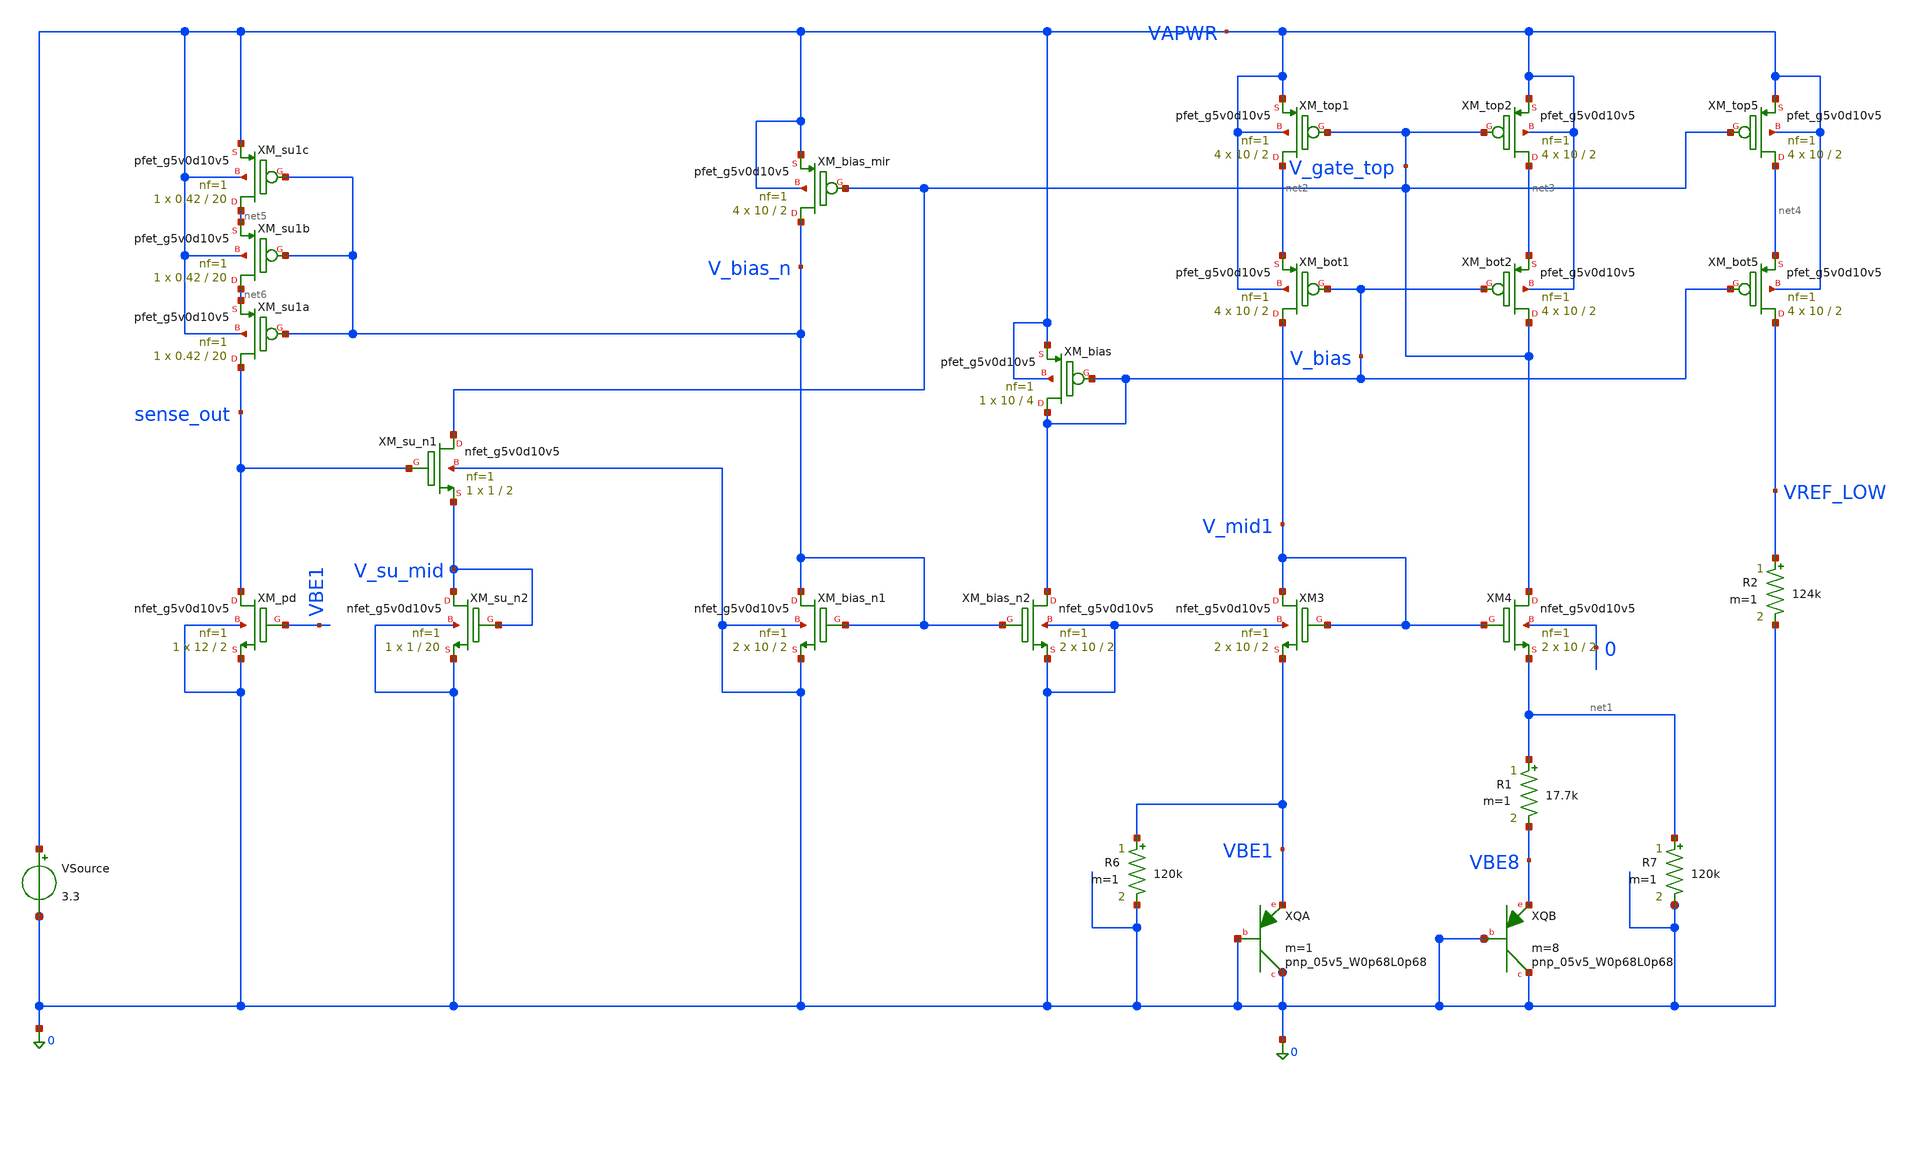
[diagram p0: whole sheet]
** sch_path: designs/bgr_ldo/sim/bgr_core_tb.sch
**.subckt bgr_core_tb
XXQA 0 0 VBE1 sky130_fd_pr__pnp_05v5_W0p68L0p68 m=1
VSource VAPWR 0 3.3
XXQB 0 0 VBE8 sky130_fd_pr__pnp_05v5_W0p68L0p68 m=8
R1 net1 VBE8 17.7k m=1
R7 net1 0 120k m=1
R6 VBE1 0 120k m=1
XXM_top1 net2 V_gate_top VAPWR VAPWR sky130_fd_pr__pfet_g5v0d10v5 L=2 W=10 nf=1 ad='int((1 + 1)/2) * 10 / 1 * 0.29'
+ as='int((1 + 2)/2) * 10 / 1 * 0.29' pd='2*int((1 + 1)/2) * (10 / 1 + 0.29)' ps='2*int((1 + 2)/2) * (10 / 1 + 0.29)'
+ nrd='0.29 / 10 ' nrs='0.29 / 10 ' sa=0 sb=0 sd=0 mult=4 m=4
XXM_top2 net3 V_gate_top VAPWR VAPWR sky130_fd_pr__pfet_g5v0d10v5 L=2 W=10 nf=1 ad='int((1 + 1)/2) * 10 / 1 * 0.29'
+ as='int((1 + 2)/2) * 10 / 1 * 0.29' pd='2*int((1 + 1)/2) * (10 / 1 + 0.29)' ps='2*int((1 + 2)/2) * (10 / 1 + 0.29)'
+ nrd='0.29 / 10 ' nrs='0.29 / 10 ' sa=0 sb=0 sd=0 mult=4 m=4
XXM_top5 net4 V_gate_top VAPWR VAPWR sky130_fd_pr__pfet_g5v0d10v5 L=2 W=10 nf=1 ad='int((1 + 1)/2) * 10 / 1 * 0.29'
+ as='int((1 + 2)/2) * 10 / 1 * 0.29' pd='2*int((1 + 1)/2) * (10 / 1 + 0.29)' ps='2*int((1 + 2)/2) * (10 / 1 + 0.29)'
+ nrd='0.29 / 10 ' nrs='0.29 / 10 ' sa=0 sb=0 sd=0 mult=4 m=4
XXM3 V_mid1 V_mid1 VBE1 0 sky130_fd_pr__nfet_g5v0d10v5 L=2 W=10 nf=1 ad='int((1 + 1)/2) * 10 / 1 * 0.29'
+ as='int((1 + 2)/2) * 10 / 1 * 0.29' pd='2*int((1 + 1)/2) * (10 / 1 + 0.29)' ps='2*int((1 + 2)/2) * (10 / 1 + 0.29)'
+ nrd='0.29 / 10 ' nrs='0.29 / 10 ' sa=0 sb=0 sd=0 mult=2 m=2
XXM4 V_gate_top V_mid1 net1 0 sky130_fd_pr__nfet_g5v0d10v5 L=2 W=10 nf=1 ad='int((1 + 1)/2) * 10 / 1 * 0.29'
+ as='int((1 + 2)/2) * 10 / 1 * 0.29' pd='2*int((1 + 1)/2) * (10 / 1 + 0.29)' ps='2*int((1 + 2)/2) * (10 / 1 + 0.29)'
+ nrd='0.29 / 10 ' nrs='0.29 / 10 ' sa=0 sb=0 sd=0 mult=2 m=2
XXM_bot1 V_mid1 V_bias net2 VAPWR sky130_fd_pr__pfet_g5v0d10v5 L=2 W=10 nf=1 ad='int((1 + 1)/2) * 10 / 1 * 0.29'
+ as='int((1 + 2)/2) * 10 / 1 * 0.29' pd='2*int((1 + 1)/2) * (10 / 1 + 0.29)' ps='2*int((1 + 2)/2) * (10 / 1 + 0.29)'
+ nrd='0.29 / 10 ' nrs='0.29 / 10 ' sa=0 sb=0 sd=0 mult=4 m=4
XXM_bot2 V_gate_top V_bias net3 VAPWR sky130_fd_pr__pfet_g5v0d10v5 L=2 W=10 nf=1 ad='int((1 + 1)/2) * 10 / 1 * 0.29'
+ as='int((1 + 2)/2) * 10 / 1 * 0.29' pd='2*int((1 + 1)/2) * (10 / 1 + 0.29)' ps='2*int((1 + 2)/2) * (10 / 1 + 0.29)'
+ nrd='0.29 / 10 ' nrs='0.29 / 10 ' sa=0 sb=0 sd=0 mult=4 m=4
XXM_bot5 VREF_LOW V_bias net4 VAPWR sky130_fd_pr__pfet_g5v0d10v5 L=2 W=10 nf=1 ad='int((1 + 1)/2) * 10 / 1 * 0.29'
+ as='int((1 + 2)/2) * 10 / 1 * 0.29' pd='2*int((1 + 1)/2) * (10 / 1 + 0.29)' ps='2*int((1 + 2)/2) * (10 / 1 + 0.29)'
+ nrd='0.29 / 10 ' nrs='0.29 / 10 ' sa=0 sb=0 sd=0 mult=4 m=4
XXM_bias V_bias V_bias VAPWR VAPWR sky130_fd_pr__pfet_g5v0d10v5 L=4 W=10 nf=1 ad='int((1 + 1)/2) * 10 / 1 * 0.29'
+ as='int((1 + 2)/2) * 10 / 1 * 0.29' pd='2*int((1 + 1)/2) * (10 / 1 + 0.29)' ps='2*int((1 + 2)/2) * (10 / 1 + 0.29)'
+ nrd='0.29 / 10 ' nrs='0.29 / 10 ' sa=0 sb=0 sd=0 mult=1 m=1
R2 VREF_LOW 0 124k m=1
XXM_bias_mir V_bias_n V_gate_top VAPWR VAPWR sky130_fd_pr__pfet_g5v0d10v5 L=2 W=10 nf=1 ad='int((1 + 1)/2) * 10 / 1 * 0.29'
+ as='int((1 + 2)/2) * 10 / 1 * 0.29' pd='2*int((1 + 1)/2) * (10 / 1 + 0.29)' ps='2*int((1 + 2)/2) * (10 / 1 + 0.29)'
+ nrd='0.29 / 10 ' nrs='0.29 / 10 ' sa=0 sb=0 sd=0 mult=4 m=4
XXM_bias_n1 V_bias_n V_bias_n 0 0 sky130_fd_pr__nfet_g5v0d10v5 L=2 W=10 nf=1 ad='int((1 + 1)/2) * 10 / 1 * 0.29'
+ as='int((1 + 2)/2) * 10 / 1 * 0.29' pd='2*int((1 + 1)/2) * (10 / 1 + 0.29)' ps='2*int((1 + 2)/2) * (10 / 1 + 0.29)'
+ nrd='0.29 / 10 ' nrs='0.29 / 10 ' sa=0 sb=0 sd=0 mult=2 m=2
XXM_bias_n2 V_bias V_bias_n 0 0 sky130_fd_pr__nfet_g5v0d10v5 L=2 W=10 nf=1 ad='int((1 + 1)/2) * 10 / 1 * 0.29'
+ as='int((1 + 2)/2) * 10 / 1 * 0.29' pd='2*int((1 + 1)/2) * (10 / 1 + 0.29)' ps='2*int((1 + 2)/2) * (10 / 1 + 0.29)'
+ nrd='0.29 / 10 ' nrs='0.29 / 10 ' sa=0 sb=0 sd=0 mult=2 m=2
XXM_su_n1 V_gate_top sense_out V_su_mid 0 sky130_fd_pr__nfet_g5v0d10v5 L=2 W=1 nf=1 ad='int((1 + 1)/2) * 1 / 1 * 0.29'
+ as='int((1 + 2)/2) * 1 / 1 * 0.29' pd='2*int((1 + 1)/2) * (1 / 1 + 0.29)' ps='2*int((1 + 2)/2) * (1 / 1 + 0.29)'
+ nrd='0.29 / 1 ' nrs='0.29 / 1 ' sa=0 sb=0 sd=0 mult=1 m=1
XXM_su_n2 V_su_mid V_su_mid 0 0 sky130_fd_pr__nfet_g5v0d10v5 L=20 W=1 nf=1 ad='int((1 + 1)/2) * 1 / 1 * 0.29'
+ as='int((1 + 2)/2) * 1 / 1 * 0.29' pd='2*int((1 + 1)/2) * (1 / 1 + 0.29)' ps='2*int((1 + 2)/2) * (1 / 1 + 0.29)'
+ nrd='0.29 / 1 ' nrs='0.29 / 1 ' sa=0 sb=0 sd=0 mult=1 m=1
XXM_pd sense_out VBE1 0 0 sky130_fd_pr__nfet_g5v0d10v5 L=2 W=12 nf=1 ad='int((1 + 1)/2) * 12 / 1 * 0.29'
+ as='int((1 + 2)/2) * 12 / 1 * 0.29' pd='2*int((1 + 1)/2) * (12 / 1 + 0.29)' ps='2*int((1 + 2)/2) * (12 / 1 + 0.29)'
+ nrd='0.29 / 12 ' nrs='0.29 / 12 ' sa=0 sb=0 sd=0 mult=1 m=1
XXM_su1a sense_out V_bias_n net6 VAPWR sky130_fd_pr__pfet_g5v0d10v5 L=20 W=0.42 nf=1 ad='int((1 + 1)/2) * 0.42 / 1 * 0.29'
+ as='int((1 + 2)/2) * 0.42 / 1 * 0.29' pd='2*int((1 + 1)/2) * (0.42 / 1 + 0.29)' ps='2*int((1 + 2)/2) * (0.42 / 1 + 0.29)'
+ nrd='0.29 / 0.42 ' nrs='0.29 / 0.42 ' sa=0 sb=0 sd=0 mult=1 m=1
XXM_su1b net6 V_bias_n net5 VAPWR sky130_fd_pr__pfet_g5v0d10v5 L=20 W=0.42 nf=1 ad='int((1 + 1)/2) * 0.42 / 1 * 0.29'
+ as='int((1 + 2)/2) * 0.42 / 1 * 0.29' pd='2*int((1 + 1)/2) * (0.42 / 1 + 0.29)' ps='2*int((1 + 2)/2) * (0.42 / 1 + 0.29)'
+ nrd='0.29 / 0.42 ' nrs='0.29 / 0.42 ' sa=0 sb=0 sd=0 mult=1 m=1
XXM_su1c net5 V_bias_n VAPWR VAPWR sky130_fd_pr__pfet_g5v0d10v5 L=20 W=0.42 nf=1 ad='int((1 + 1)/2) * 0.42 / 1 * 0.29'
+ as='int((1 + 2)/2) * 0.42 / 1 * 0.29' pd='2*int((1 + 1)/2) * (0.42 / 1 + 0.29)' ps='2*int((1 + 2)/2) * (0.42 / 1 + 0.29)'
+ nrd='0.29 / 0.42 ' nrs='0.29 / 0.42 ' sa=0 sb=0 sd=0 mult=1 m=1
**** begin user architecture code

.save all @m.xxm_su_n1.msky130_fd_pr__nfet_g5v0d10v5[id]
.dc temp -40 125 5

.control
  tran 10n 10u uic
  echo ===== TEST D: power-up =====
  plot v(vapwr) v(vref_low)
  plot v(sense_out) v(v_bias_n) v(v_gate_top)
  write startup_tran.raw
.endc


** opencircuitdesign pdks install
.lib $::SKYWATER_MODELS/sky130.lib.spice tt

**** end user architecture code
**.ends
.end
